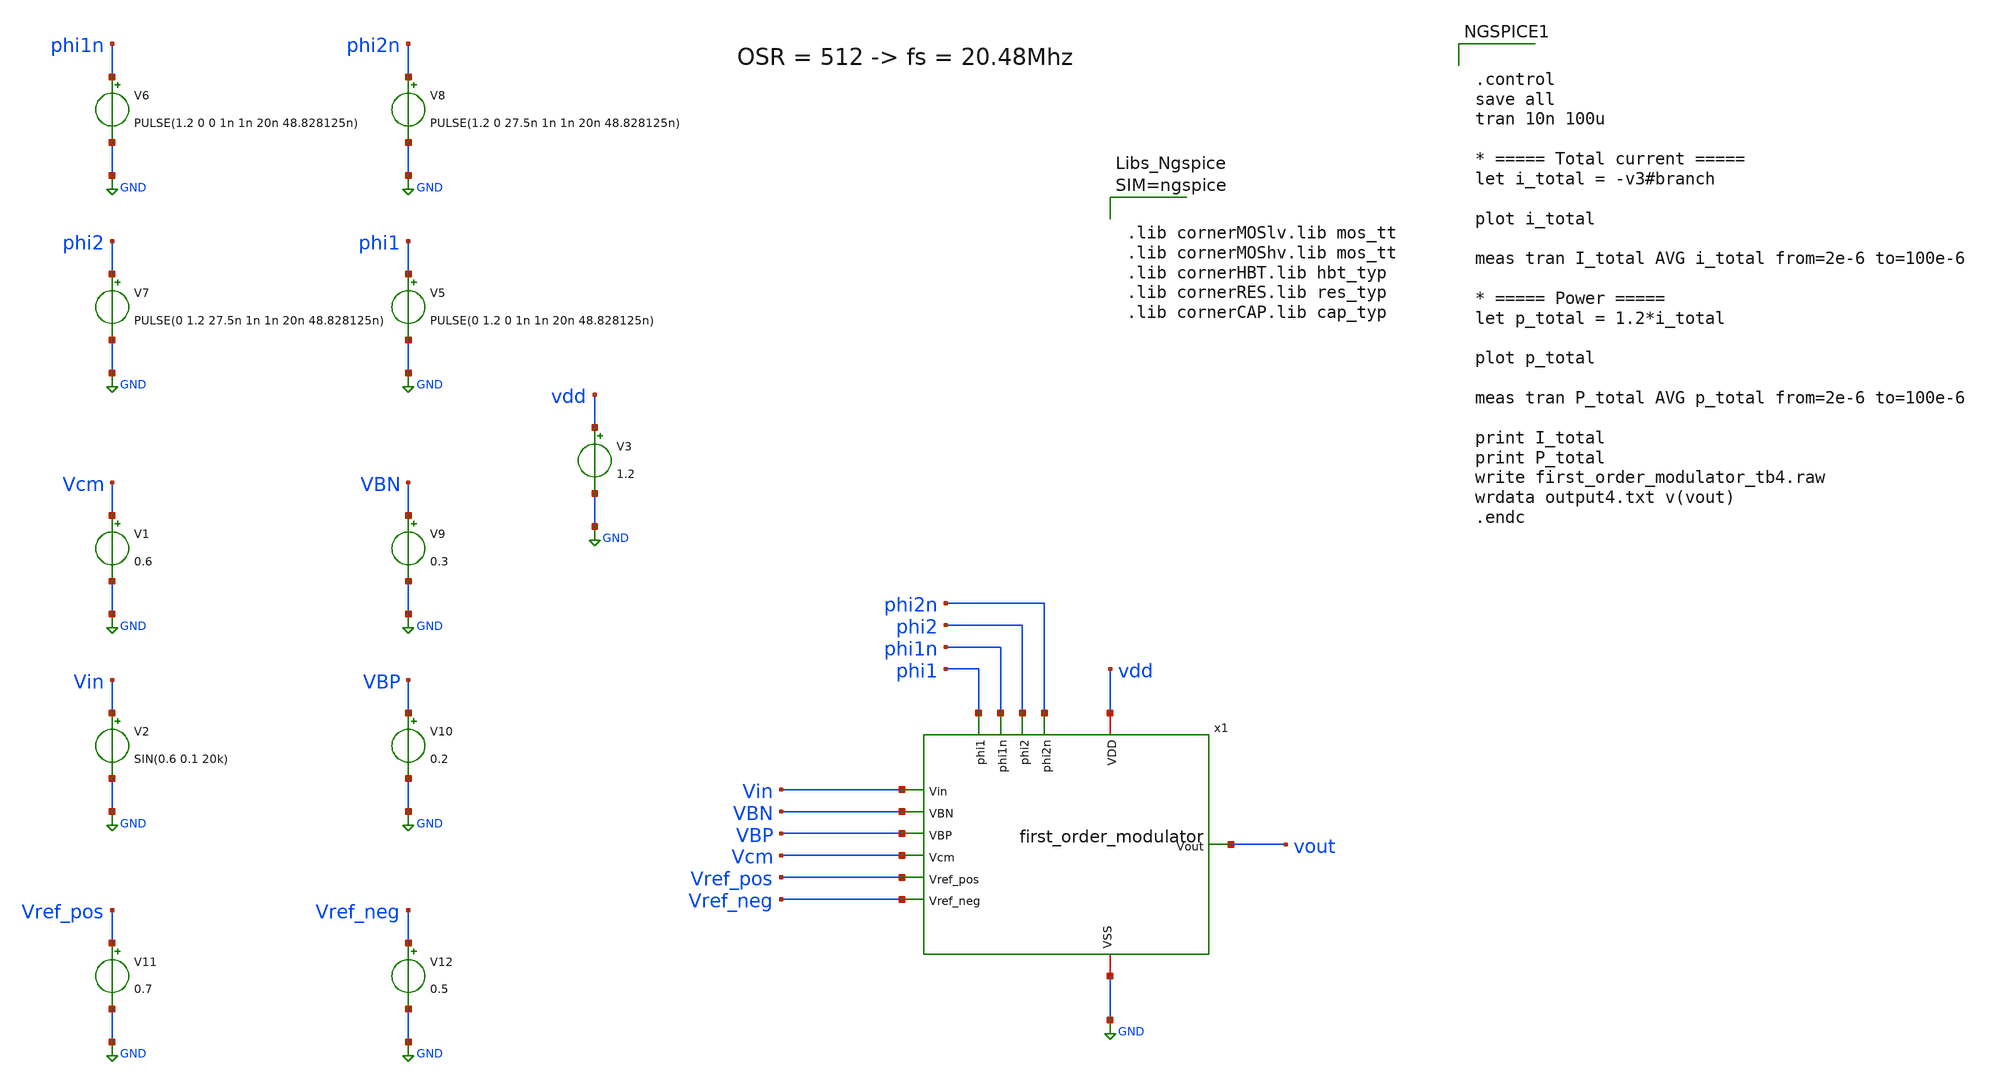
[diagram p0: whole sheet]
** sch_path: xschem/first_order_modulator_tb4.sch
**.subckt first_order_modulator_tb4
V5 phi1 GND PULSE(0 1.2 0 1n 1n 20n 48.828125n)
V6 phi1n GND PULSE(1.2 0 0 1n 1n 20n 48.828125n)
V7 phi2 GND PULSE(0 1.2 27.5n 1n 1n 20n 48.828125n)
V8 phi2n GND PULSE(1.2 0 27.5n 1n 1n 20n 48.828125n)
V1 Vcm GND 0.6
V2 Vin GND SIN(0.6 0.1 20k)
V3 vdd GND 1.2
V9 VBN GND 0.3
V10 VBP GND 0.2
V12 Vref_neg GND 0.5
V11 Vref_pos GND 0.7
x1 Vin VBN VBP Vcm Vref_pos Vref_neg phi1 phi1n phi2 phi2n vdd GND vout first_order_modulator
**** begin user architecture code



.lib cornerMOSlv.lib mos_tt
.lib cornerMOShv.lib mos_tt
.lib cornerHBT.lib hbt_typ
.lib cornerRES.lib res_typ
.lib cornerCAP.lib cap_typ





.control
save all
tran 10n 100u

* ===== Total current =====
let i_total = -v3#branch

plot i_total

meas tran I_total AVG i_total from=2e-6 to=100e-6

* ===== Power =====
let p_total = 1.2*i_total

plot p_total

meas tran P_total AVG p_total from=2e-6 to=100e-6

print I_total
print P_total
write first_order_modulator_tb4.raw
wrdata output4.txt v(vout)
.endc


**** end user architecture code
**.ends
.GLOBAL GND
.end
